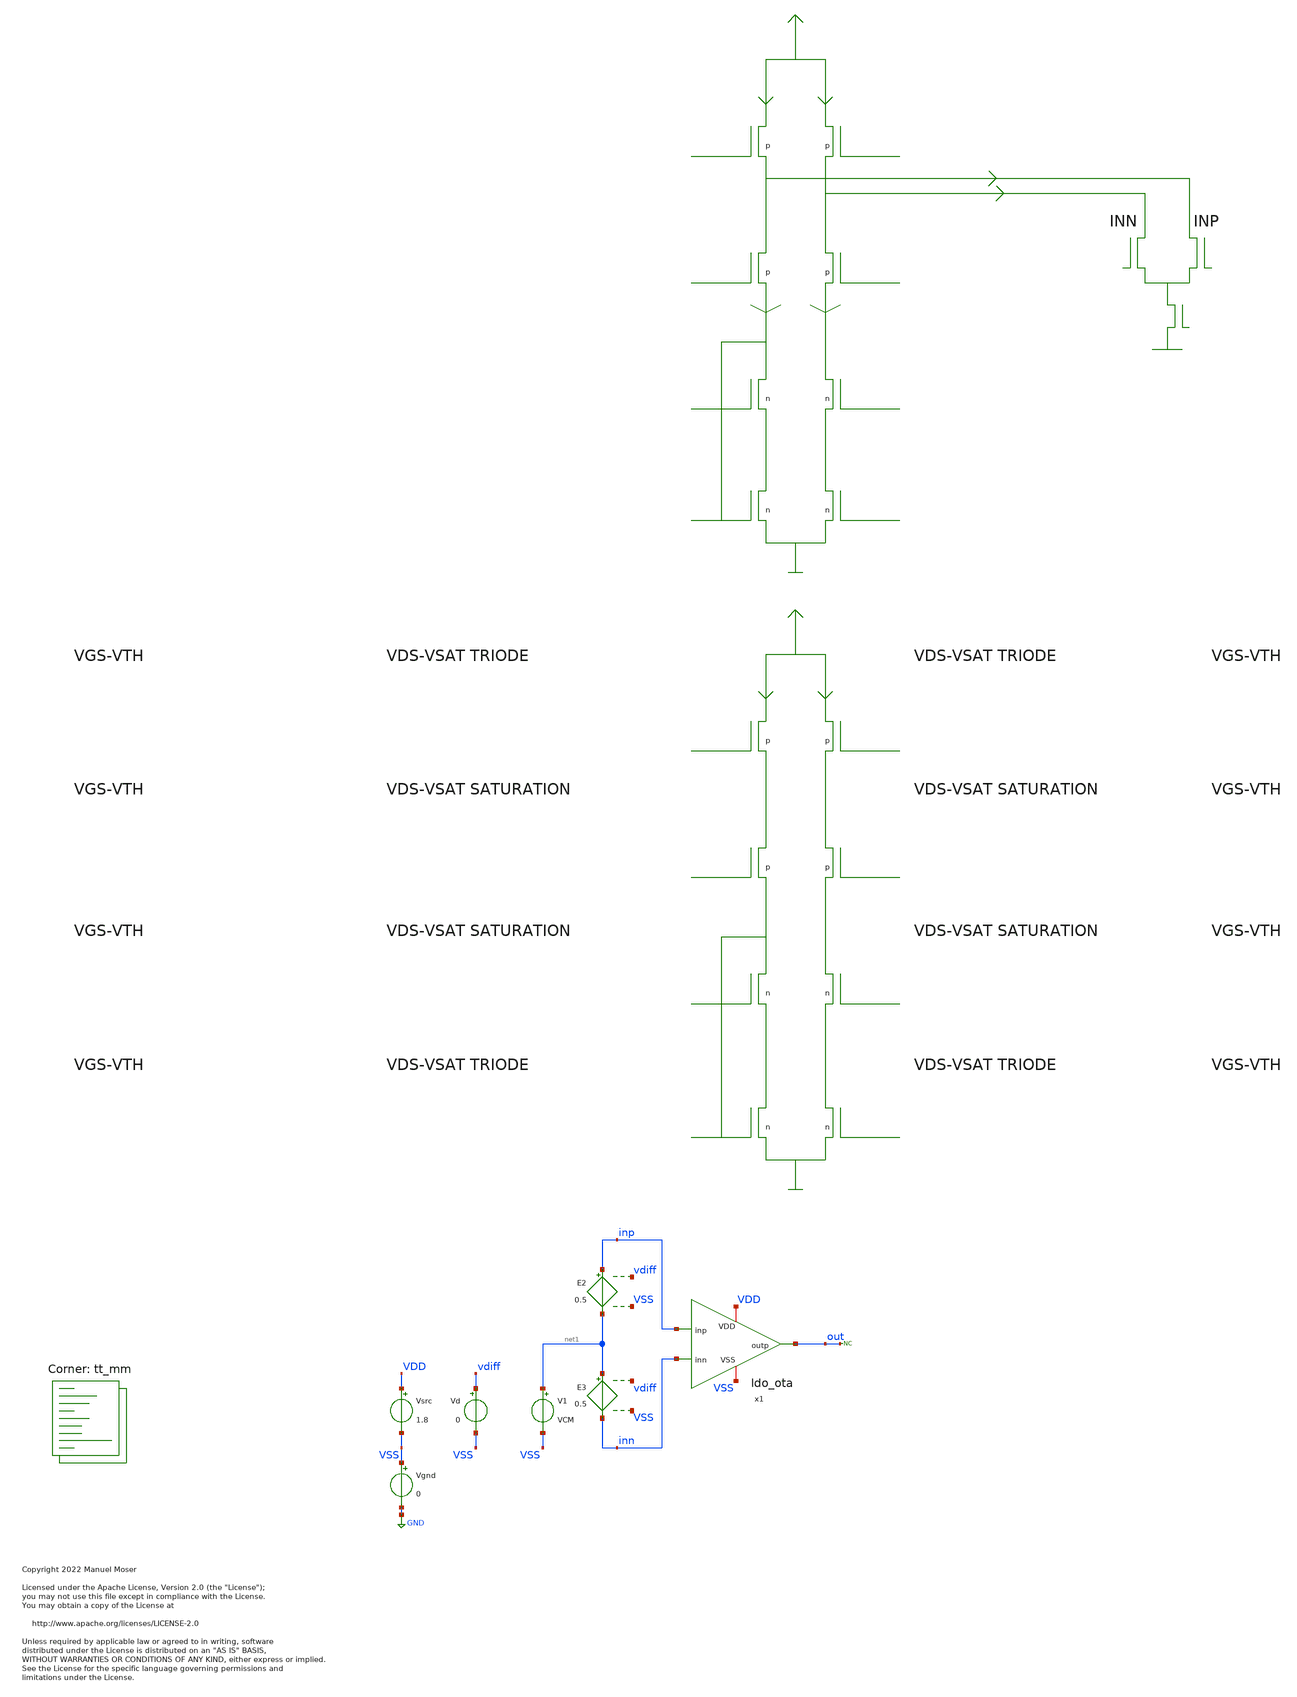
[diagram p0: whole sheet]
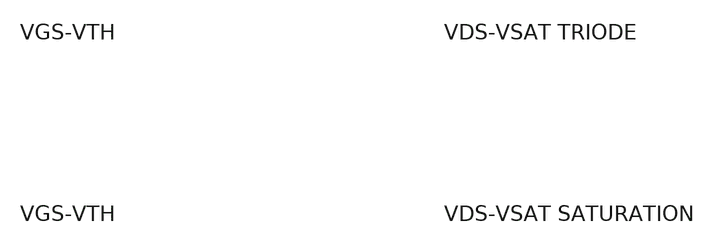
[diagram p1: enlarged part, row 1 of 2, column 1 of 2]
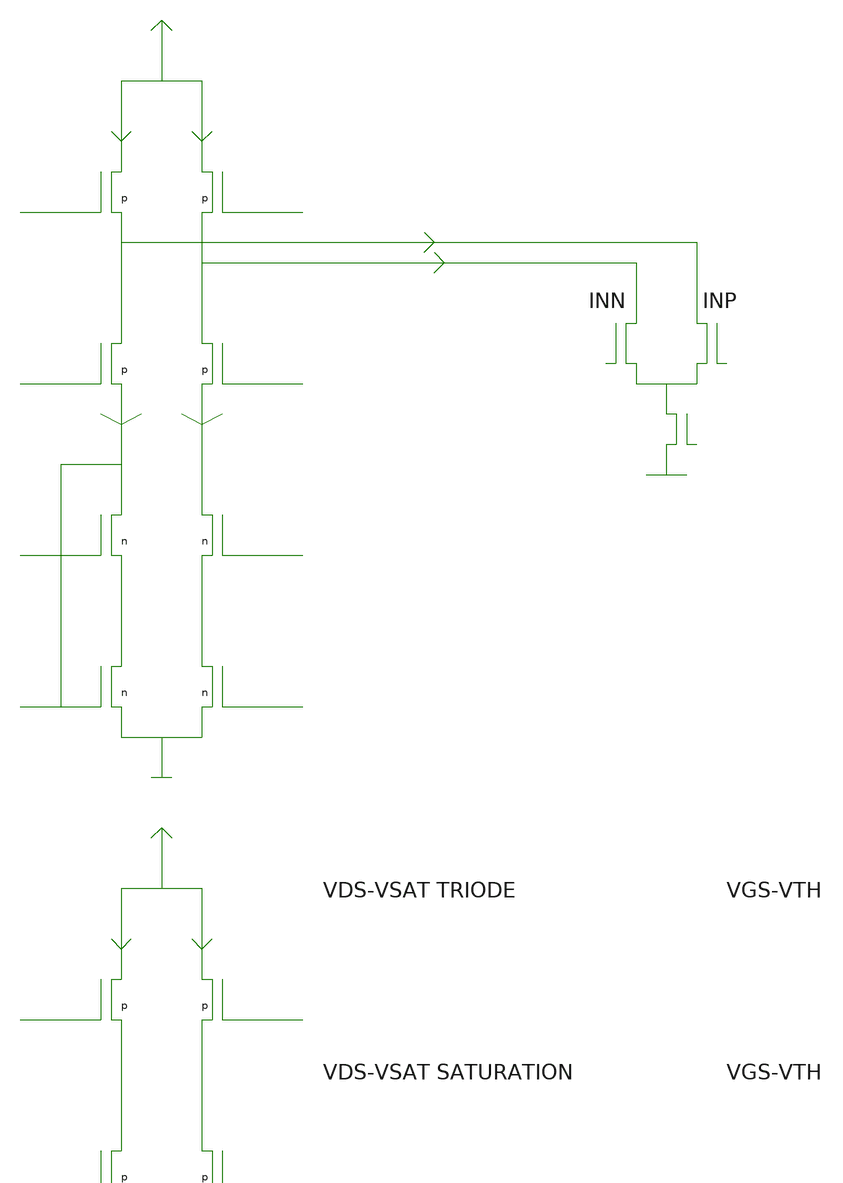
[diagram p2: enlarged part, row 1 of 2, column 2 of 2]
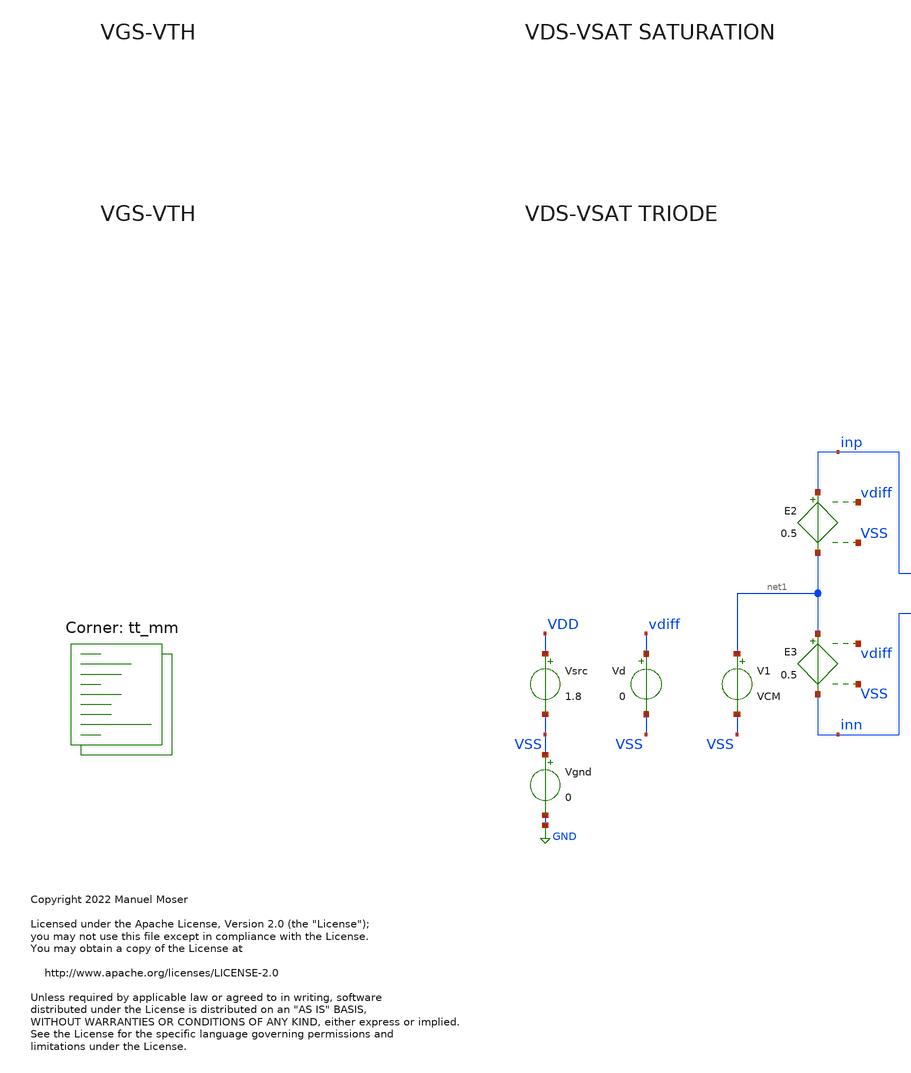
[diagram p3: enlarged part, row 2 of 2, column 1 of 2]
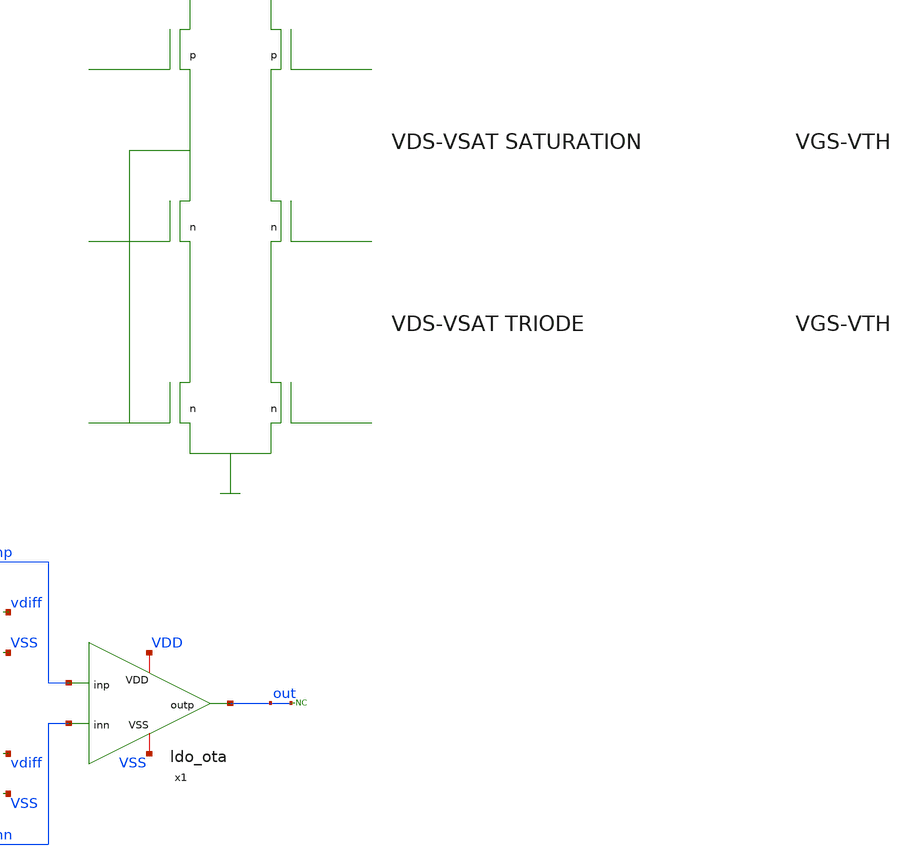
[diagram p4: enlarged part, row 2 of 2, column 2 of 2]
** sch_path: xschem/ldo_ota_tb.sch
* Copyright 2022 Manuel Moser
* Licensed under the Apache License, Version 2.0 (the "License");
**.subckt ldo_ota_tb
x1 VDD inp out inn VSS ldo_ota
V1 net1 VSS VCM
Vd vdiff VSS 0
Vsrc VDD VSS 1.8
* noconn out
E2 inp net1 vdiff VSS 0.5
E3 net1 inn vdiff VSS 0.5
Vgnd VSS GND 0
**** begin user architecture code



.temp 27
.options savecurrents

.param vcm = 0.9

.save all
 + @m.x1.x1.xmn1.msky130_fd_pr__nfet_01v8_lvt[vgs] @m.x1.x1.xmn1.msky130_fd_pr__nfet_01v8_lvt[vth]
+ @m.x1.x1.xmn1.msky130_fd_pr__nfet_01v8_lvt[vds] @m.x1.x1.xmn1.msky130_fd_pr__nfet_01v8_lvt[vdsat] @m.x1.x1.xmn1.msky130_fd_pr__nfet_01v8_lvt[id]
 + @m.x1.x1.xmn2.msky130_fd_pr__nfet_01v8_lvt[vgs] @m.x1.x1.xmn2.msky130_fd_pr__nfet_01v8_lvt[vth]
+ @m.x1.x1.xmn2.msky130_fd_pr__nfet_01v8_lvt[vds] @m.x1.x1.xmn2.msky130_fd_pr__nfet_01v8_lvt[vdsat] @m.x1.x1.xmn2.msky130_fd_pr__nfet_01v8_lvt[id]
 + @m.x1.x1.xmn3.msky130_fd_pr__nfet_01v8_lvt[vgs] @m.x1.x1.xmn3.msky130_fd_pr__nfet_01v8_lvt[vth]
+ @m.x1.x1.xmn3.msky130_fd_pr__nfet_01v8_lvt[vds] @m.x1.x1.xmn3.msky130_fd_pr__nfet_01v8_lvt[vdsat] @m.x1.x1.xmn3.msky130_fd_pr__nfet_01v8_lvt[id]
 + @m.x1.x1.xmn4.msky130_fd_pr__nfet_01v8_lvt[vgs] @m.x1.x1.xmn4.msky130_fd_pr__nfet_01v8_lvt[vth]
+ @m.x1.x1.xmn4.msky130_fd_pr__nfet_01v8_lvt[vds] @m.x1.x1.xmn4.msky130_fd_pr__nfet_01v8_lvt[vdsat] @m.x1.x1.xmn4.msky130_fd_pr__nfet_01v8_lvt[id]
 + @m.x1.x1.xmn5.msky130_fd_pr__nfet_01v8_lvt[vgs] @m.x1.x1.xmn5.msky130_fd_pr__nfet_01v8_lvt[vth]
+ @m.x1.x1.xmn5.msky130_fd_pr__nfet_01v8_lvt[vds] @m.x1.x1.xmn5.msky130_fd_pr__nfet_01v8_lvt[vdsat] @m.x1.x1.xmn5.msky130_fd_pr__nfet_01v8_lvt[id]
 + @m.x1.x1.xmn6.msky130_fd_pr__nfet_01v8_lvt[vgs] @m.x1.x1.xmn6.msky130_fd_pr__nfet_01v8_lvt[vth]
+ @m.x1.x1.xmn6.msky130_fd_pr__nfet_01v8_lvt[vds] @m.x1.x1.xmn6.msky130_fd_pr__nfet_01v8_lvt[vdsat] @m.x1.x1.xmn6.msky130_fd_pr__nfet_01v8_lvt[id]
 + @m.x1.x1.xmn7.msky130_fd_pr__nfet_01v8_lvt[vgs] @m.x1.x1.xmn7.msky130_fd_pr__nfet_01v8_lvt[vth]
+ @m.x1.x1.xmn7.msky130_fd_pr__nfet_01v8_lvt[vds] @m.x1.x1.xmn7.msky130_fd_pr__nfet_01v8_lvt[vdsat] @m.x1.x1.xmn7.msky130_fd_pr__nfet_01v8_lvt[id]
 + @m.x1.x1.xmp1.msky130_fd_pr__pfet_01v8_lvt[vgs] @m.x1.x1.xmp1.msky130_fd_pr__pfet_01v8_lvt[vth]
+ @m.x1.x1.xmp1.msky130_fd_pr__pfet_01v8_lvt[vds] @m.x1.x1.xmp1.msky130_fd_pr__pfet_01v8_lvt[vdsat] @m.x1.x1.xmp1.msky130_fd_pr__pfet_01v8_lvt[id]
 + @m.x1.x1.xmp2.msky130_fd_pr__pfet_01v8_lvt[vgs] @m.x1.x1.xmp2.msky130_fd_pr__pfet_01v8_lvt[vth]
+ @m.x1.x1.xmp2.msky130_fd_pr__pfet_01v8_lvt[vds] @m.x1.x1.xmp2.msky130_fd_pr__pfet_01v8_lvt[vdsat] @m.x1.x1.xmp2.msky130_fd_pr__pfet_01v8_lvt[id]
 + @m.x1.x1.xmp3.msky130_fd_pr__pfet_01v8_lvt[vgs] @m.x1.x1.xmp3.msky130_fd_pr__pfet_01v8_lvt[vth]
+ @m.x1.x1.xmp3.msky130_fd_pr__pfet_01v8_lvt[vds] @m.x1.x1.xmp3.msky130_fd_pr__pfet_01v8_lvt[vdsat] @m.x1.x1.xmp3.msky130_fd_pr__pfet_01v8_lvt[id]
 + @m.x1.x1.xmp4.msky130_fd_pr__pfet_01v8_lvt[vgs] @m.x1.x1.xmp4.msky130_fd_pr__pfet_01v8_lvt[vth]
+ @m.x1.x1.xmp4.msky130_fd_pr__pfet_01v8_lvt[vds] @m.x1.x1.xmp4.msky130_fd_pr__pfet_01v8_lvt[vdsat] @m.x1.x1.xmp4.msky130_fd_pr__pfet_01v8_lvt[id]

.control
set num_threads = 12
write results.raw
set appendwrite

repeat 20
  reset
  dc vd -50m 50m 0.1m temp -30 60 90
  *dc temp -30 60 1

write results.raw out x1.bias1 x1.bias2 x1.bias3 x1.bias4
 + @m.x1.x1.xmn1.msky130_fd_pr__nfet_01v8_lvt[vgs] @m.x1.x1.xmn1.msky130_fd_pr__nfet_01v8_lvt[vth]
+ @m.x1.x1.xmn1.msky130_fd_pr__nfet_01v8_lvt[vds] @m.x1.x1.xmn1.msky130_fd_pr__nfet_01v8_lvt[vdsat] @m.x1.x1.xmn1.msky130_fd_pr__nfet_01v8_lvt[id]
 + @m.x1.x1.xmn2.msky130_fd_pr__nfet_01v8_lvt[vgs] @m.x1.x1.xmn2.msky130_fd_pr__nfet_01v8_lvt[vth]
+ @m.x1.x1.xmn2.msky130_fd_pr__nfet_01v8_lvt[vds] @m.x1.x1.xmn2.msky130_fd_pr__nfet_01v8_lvt[vdsat] @m.x1.x1.xmn2.msky130_fd_pr__nfet_01v8_lvt[id]
 + @m.x1.x1.xmn3.msky130_fd_pr__nfet_01v8_lvt[vgs] @m.x1.x1.xmn3.msky130_fd_pr__nfet_01v8_lvt[vth]
+ @m.x1.x1.xmn3.msky130_fd_pr__nfet_01v8_lvt[vds] @m.x1.x1.xmn3.msky130_fd_pr__nfet_01v8_lvt[vdsat] @m.x1.x1.xmn3.msky130_fd_pr__nfet_01v8_lvt[id]
 + @m.x1.x1.xmn4.msky130_fd_pr__nfet_01v8_lvt[vgs] @m.x1.x1.xmn4.msky130_fd_pr__nfet_01v8_lvt[vth]
+ @m.x1.x1.xmn4.msky130_fd_pr__nfet_01v8_lvt[vds] @m.x1.x1.xmn4.msky130_fd_pr__nfet_01v8_lvt[vdsat] @m.x1.x1.xmn4.msky130_fd_pr__nfet_01v8_lvt[id]
 + @m.x1.x1.xmn5.msky130_fd_pr__nfet_01v8_lvt[vgs] @m.x1.x1.xmn5.msky130_fd_pr__nfet_01v8_lvt[vth]
+ @m.x1.x1.xmn5.msky130_fd_pr__nfet_01v8_lvt[vds] @m.x1.x1.xmn5.msky130_fd_pr__nfet_01v8_lvt[vdsat] @m.x1.x1.xmn5.msky130_fd_pr__nfet_01v8_lvt[id]
 + @m.x1.x1.xmn6.msky130_fd_pr__nfet_01v8_lvt[vgs] @m.x1.x1.xmn6.msky130_fd_pr__nfet_01v8_lvt[vth]
+ @m.x1.x1.xmn6.msky130_fd_pr__nfet_01v8_lvt[vds] @m.x1.x1.xmn6.msky130_fd_pr__nfet_01v8_lvt[vdsat] @m.x1.x1.xmn6.msky130_fd_pr__nfet_01v8_lvt[id]
 + @m.x1.x1.xmn7.msky130_fd_pr__nfet_01v8_lvt[vgs] @m.x1.x1.xmn7.msky130_fd_pr__nfet_01v8_lvt[vth]
+ @m.x1.x1.xmn7.msky130_fd_pr__nfet_01v8_lvt[vds] @m.x1.x1.xmn7.msky130_fd_pr__nfet_01v8_lvt[vdsat] @m.x1.x1.xmn7.msky130_fd_pr__nfet_01v8_lvt[id]
 + @m.x1.x1.xmp1.msky130_fd_pr__pfet_01v8_lvt[vgs] @m.x1.x1.xmp1.msky130_fd_pr__pfet_01v8_lvt[vth]
+ @m.x1.x1.xmp1.msky130_fd_pr__pfet_01v8_lvt[vds] @m.x1.x1.xmp1.msky130_fd_pr__pfet_01v8_lvt[vdsat] @m.x1.x1.xmp1.msky130_fd_pr__pfet_01v8_lvt[id]
 + @m.x1.x1.xmp2.msky130_fd_pr__pfet_01v8_lvt[vgs] @m.x1.x1.xmp2.msky130_fd_pr__pfet_01v8_lvt[vth]
+ @m.x1.x1.xmp2.msky130_fd_pr__pfet_01v8_lvt[vds] @m.x1.x1.xmp2.msky130_fd_pr__pfet_01v8_lvt[vdsat] @m.x1.x1.xmp2.msky130_fd_pr__pfet_01v8_lvt[id]
 + @m.x1.x1.xmp3.msky130_fd_pr__pfet_01v8_lvt[vgs] @m.x1.x1.xmp3.msky130_fd_pr__pfet_01v8_lvt[vth]
+ @m.x1.x1.xmp3.msky130_fd_pr__pfet_01v8_lvt[vds] @m.x1.x1.xmp3.msky130_fd_pr__pfet_01v8_lvt[vdsat] @m.x1.x1.xmp3.msky130_fd_pr__pfet_01v8_lvt[id]
 + @m.x1.x1.xmp4.msky130_fd_pr__pfet_01v8_lvt[vgs] @m.x1.x1.xmp4.msky130_fd_pr__pfet_01v8_lvt[vth]
+ @m.x1.x1.xmp4.msky130_fd_pr__pfet_01v8_lvt[vds] @m.x1.x1.xmp4.msky130_fd_pr__pfet_01v8_lvt[vdsat] @m.x1.x1.xmp4.msky130_fd_pr__pfet_01v8_lvt[id]


end

.endc




.lib $::SKYWATER_MODELS/sky130.lib.spice tt_mm
**** end user architecture code
**.ends

* expanding   symbol:  ldo_ota.sym # of pins=5
** sym_path: xschem/ldo_ota.sym
** sch_path: xschem/ldo_ota.sch
.subckt ldo_ota VDD inp outp inn VSS
*.iopin VDD
*.iopin VSS
*.ipin inp
*.ipin inn
*.opin outp
x1 VDD inp inn bias1 bias2 bias3 outp VSS bias4 ldo_fc
x2 net1 bias2 VDD VSS bias1 net6 ldo_isource
XM10 net2 bias2 VDD VDD sky130_fd_pr__pfet_01v8_lvt L=8 W='0.55 * 1 ' nf=1 ad='int((nf+1)/2) * W / nf * 0.29'
+ as='int((nf+2)/2) * W / nf * 0.29' pd='2*int((nf+1)/2) * (W / nf + 0.29)' ps='2*int((nf+2)/2) * (W / nf + 0.29)'
+ nrd='0.29 / W ' nrs='0.29 / W ' sa=0 sb=0 sd=0 mult=1 m=1
XM12 bias2 bias2 net2 VDD sky130_fd_pr__pfet_01v8_lvt L=8 W='0.55 * 9 ' nf=9 ad='int((nf+1)/2) * W / nf * 0.29'
+ as='int((nf+2)/2) * W / nf * 0.29' pd='2*int((nf+1)/2) * (W / nf + 0.29)' ps='2*int((nf+2)/2) * (W / nf + 0.29)'
+ nrd='0.29 / W ' nrs='0.29 / W ' sa=0 sb=0 sd=0 mult=1 m=1
* noconn #net1
XM1 net3 bias1 VDD VDD sky130_fd_pr__pfet_01v8_lvt L=8 W='0.55 * 3 ' nf=3 ad='int((nf+1)/2) * W / nf * 0.29'
+ as='int((nf+2)/2) * W / nf * 0.29' pd='2*int((nf+1)/2) * (W / nf + 0.29)' ps='2*int((nf+2)/2) * (W / nf + 0.29)'
+ nrd='0.29 / W ' nrs='0.29 / W ' sa=0 sb=0 sd=0 mult=1 m=1
XM2 bias1 bias2 net3 VDD sky130_fd_pr__pfet_01v8_lvt L=8 W='0.55 * 9 ' nf=9 ad='int((nf+1)/2) * W / nf * 0.29'
+ as='int((nf+2)/2) * W / nf * 0.29' pd='2*int((nf+1)/2) * (W / nf + 0.29)' ps='2*int((nf+2)/2) * (W / nf + 0.29)'
+ nrd='0.29 / W ' nrs='0.29 / W ' sa=0 sb=0 sd=0 mult=1 m=1
XM3 net4 bias1 VDD VDD sky130_fd_pr__pfet_01v8_lvt L=8 W='0.55 * 3 ' nf=3 ad='int((nf+1)/2) * W / nf * 0.29'
+ as='int((nf+2)/2) * W / nf * 0.29' pd='2*int((nf+1)/2) * (W / nf + 0.29)' ps='2*int((nf+2)/2) * (W / nf + 0.29)'
+ nrd='0.29 / W ' nrs='0.29 / W ' sa=0 sb=0 sd=0 mult=1 m=1
XM4 bias3 bias2 net4 VDD sky130_fd_pr__pfet_01v8_lvt L=8 W='0.55 * 9 ' nf=9 ad='int((nf+1)/2) * W / nf * 0.29'
+ as='int((nf+2)/2) * W / nf * 0.29' pd='2*int((nf+1)/2) * (W / nf + 0.29)' ps='2*int((nf+2)/2) * (W / nf + 0.29)'
+ nrd='0.29 / W ' nrs='0.29 / W ' sa=0 sb=0 sd=0 mult=1 m=1
XM5 net5 bias1 VDD VDD sky130_fd_pr__pfet_01v8_lvt L=8 W='0.55 * 3 ' nf=3 ad='int((nf+1)/2) * W / nf * 0.29'
+ as='int((nf+2)/2) * W / nf * 0.29' pd='2*int((nf+1)/2) * (W / nf + 0.29)' ps='2*int((nf+2)/2) * (W / nf + 0.29)'
+ nrd='0.29 / W ' nrs='0.29 / W ' sa=0 sb=0 sd=0 mult=1 m=1
XM8 bias4 bias2 net5 VDD sky130_fd_pr__pfet_01v8_lvt L=8 W='0.55 * 9 ' nf=9 ad='int((nf+1)/2) * W / nf * 0.29'
+ as='int((nf+2)/2) * W / nf * 0.29' pd='2*int((nf+1)/2) * (W / nf + 0.29)' ps='2*int((nf+2)/2) * (W / nf + 0.29)'
+ nrd='0.29 / W ' nrs='0.29 / W ' sa=0 sb=0 sd=0 mult=1 m=1
* noconn #net6
XM9 bias3 bias3 net7 VSS sky130_fd_pr__nfet_01v8_lvt L=4 W='0.55 * 9 ' nf=9 ad='int((nf+1)/2) * W / nf * 0.29'
+ as='int((nf+2)/2) * W / nf * 0.29' pd='2*int((nf+1)/2) * (W / nf + 0.29)' ps='2*int((nf+2)/2) * (W / nf + 0.29)'
+ nrd='0.29 / W ' nrs='0.29 / W ' sa=0 sb=0 sd=0 mult=1 m=1
XM11 net7 bias3 VSS VSS sky130_fd_pr__nfet_01v8_lvt L=4 W='0.55 * 1 ' nf=1 ad='int((nf+1)/2) * W / nf * 0.29'
+ as='int((nf+2)/2) * W / nf * 0.29' pd='2*int((nf+1)/2) * (W / nf + 0.29)' ps='2*int((nf+2)/2) * (W / nf + 0.29)'
+ nrd='0.29 / W ' nrs='0.29 / W ' sa=0 sb=0 sd=0 mult=1 m=1
XM13 bias4 bias3 net8 VSS sky130_fd_pr__nfet_01v8_lvt L=4 W='0.55 * 9 ' nf=9 ad='int((nf+1)/2) * W / nf * 0.29'
+ as='int((nf+2)/2) * W / nf * 0.29' pd='2*int((nf+1)/2) * (W / nf + 0.29)' ps='2*int((nf+2)/2) * (W / nf + 0.29)'
+ nrd='0.29 / W ' nrs='0.29 / W ' sa=0 sb=0 sd=0 mult=1 m=1
XM14 net8 bias4 VSS VSS sky130_fd_pr__nfet_01v8_lvt L=4 W='0.55 * 3 ' nf=3 ad='int((nf+1)/2) * W / nf * 0.29'
+ as='int((nf+2)/2) * W / nf * 0.29' pd='2*int((nf+1)/2) * (W / nf + 0.29)' ps='2*int((nf+2)/2) * (W / nf + 0.29)'
+ nrd='0.29 / W ' nrs='0.29 / W ' sa=0 sb=0 sd=0 mult=1 m=1
.ends


* expanding   symbol:  ldo_fc.sym # of pins=9
** sym_path: xschem/ldo_fc.sym
** sch_path: xschem/ldo_fc.sch
.subckt ldo_fc VDD inp inn bias1 bias2 bias3 outp VSS bias4
*.iopin VSS
*.iopin VDD
*.ipin inp
*.ipin inn
*.ipin bias1
*.opin outp
*.ipin bias2
*.ipin bias3
*.ipin bias4
XMN4 outp bias3 net1 VSS sky130_fd_pr__nfet_01v8_lvt L=4 W='0.55 * 9 ' nf=9 ad='int((nf+1)/2) * W / nf * 0.29'
+ as='int((nf+2)/2) * W / nf * 0.29' pd='2*int((nf+1)/2) * (W / nf + 0.29)' ps='2*int((nf+2)/2) * (W / nf + 0.29)'
+ nrd='0.29 / W ' nrs='0.29 / W ' sa=0 sb=0 sd=0 mult=8 m=8
XMN7 net1 net3 VSS VSS sky130_fd_pr__nfet_01v8_lvt L=4 W='0.55 * 3 ' nf=3 ad='int((nf+1)/2) * W / nf * 0.29'
+ as='int((nf+2)/2) * W / nf * 0.29' pd='2*int((nf+1)/2) * (W / nf + 0.29)' ps='2*int((nf+2)/2) * (W / nf + 0.29)'
+ nrd='0.29 / W ' nrs='0.29 / W ' sa=0 sb=0 sd=0 mult=8 m=8
XMN3 net3 bias3 net2 VSS sky130_fd_pr__nfet_01v8_lvt L=4 W='0.55 * 9 ' nf=9 ad='int((nf+1)/2) * W / nf * 0.29'
+ as='int((nf+2)/2) * W / nf * 0.29' pd='2*int((nf+1)/2) * (W / nf + 0.29)' ps='2*int((nf+2)/2) * (W / nf + 0.29)'
+ nrd='0.29 / W ' nrs='0.29 / W ' sa=0 sb=0 sd=0 mult=8 m=8
XMN6 net2 net3 VSS VSS sky130_fd_pr__nfet_01v8_lvt L=4 W='0.55 * 3 ' nf=3 ad='int((nf+1)/2) * W / nf * 0.29'
+ as='int((nf+2)/2) * W / nf * 0.29' pd='2*int((nf+1)/2) * (W / nf + 0.29)' ps='2*int((nf+2)/2) * (W / nf + 0.29)'
+ nrd='0.29 / W ' nrs='0.29 / W ' sa=0 sb=0 sd=0 mult=8 m=8
XMP4 outp bias2 net5 VDD sky130_fd_pr__pfet_01v8_lvt L=8 W='0.55 * 9 ' nf=9 ad='int((nf+1)/2) * W / nf * 0.29'
+ as='int((nf+2)/2) * W / nf * 0.29' pd='2*int((nf+1)/2) * (W / nf + 0.29)' ps='2*int((nf+2)/2) * (W / nf + 0.29)'
+ nrd='0.29 / W ' nrs='0.29 / W ' sa=0 sb=0 sd=0 mult=8 m=8
XMP2 net5 bias1 VDD VDD sky130_fd_pr__pfet_01v8_lvt L=8 W='0.55 * 3 ' nf=3 ad='int((nf+1)/2) * W / nf * 0.29'
+ as='int((nf+2)/2) * W / nf * 0.29' pd='2*int((nf+1)/2) * (W / nf + 0.29)' ps='2*int((nf+2)/2) * (W / nf + 0.29)'
+ nrd='0.29 / W ' nrs='0.29 / W ' sa=0 sb=0 sd=0 mult=15 m=15
XMP3 net3 bias2 net4 VDD sky130_fd_pr__pfet_01v8_lvt L=8 W='0.55 * 9 ' nf=9 ad='int((nf+1)/2) * W / nf * 0.29'
+ as='int((nf+2)/2) * W / nf * 0.29' pd='2*int((nf+1)/2) * (W / nf + 0.29)' ps='2*int((nf+2)/2) * (W / nf + 0.29)'
+ nrd='0.29 / W ' nrs='0.29 / W ' sa=0 sb=0 sd=0 mult=8 m=8
XMP1 net4 bias1 VDD VDD sky130_fd_pr__pfet_01v8_lvt L=8 W='0.55 * 3 ' nf=3 ad='int((nf+1)/2) * W / nf * 0.29'
+ as='int((nf+2)/2) * W / nf * 0.29' pd='2*int((nf+1)/2) * (W / nf + 0.29)' ps='2*int((nf+2)/2) * (W / nf + 0.29)'
+ nrd='0.29 / W ' nrs='0.29 / W ' sa=0 sb=0 sd=0 mult=15 m=15
XMN5 net6 bias4 VSS VSS sky130_fd_pr__nfet_01v8_lvt L=4 W='0.55 * 3 ' nf=3 ad='int((nf+1)/2) * W / nf * 0.29'
+ as='int((nf+2)/2) * W / nf * 0.29' pd='2*int((nf+1)/2) * (W / nf + 0.29)' ps='2*int((nf+2)/2) * (W / nf + 0.29)'
+ nrd='0.29 / W ' nrs='0.29 / W ' sa=0 sb=0 sd=0 mult=14 m=14
XMN1 net4 inp net6 VSS sky130_fd_pr__nfet_01v8_lvt L=0.25 W='7 * 20 ' nf=20 ad='int((nf+1)/2) * W / nf * 0.29'
+ as='int((nf+2)/2) * W / nf * 0.29' pd='2*int((nf+1)/2) * (W / nf + 0.29)' ps='2*int((nf+2)/2) * (W / nf + 0.29)'
+ nrd='0.29 / W ' nrs='0.29 / W ' sa=0 sb=0 sd=0 mult=1 m=1
XMN2 net5 inn net6 VSS sky130_fd_pr__nfet_01v8_lvt L=0.25 W='7 * 20 ' nf=20 ad='int((nf+1)/2) * W / nf * 0.29'
+ as='int((nf+2)/2) * W / nf * 0.29' pd='2*int((nf+1)/2) * (W / nf + 0.29)' ps='2*int((nf+2)/2) * (W / nf + 0.29)'
+ nrd='0.29 / W ' nrs='0.29 / W ' sa=0 sb=0 sd=0 mult=1 m=1
.ends


* expanding   symbol:  ldo_isource.sym # of pins=6
** sym_path: xschem/ldo_isource.sym
** sch_path: xschem/ldo_isource.sch
.subckt ldo_isource curr_p2 curr_n1 VDD VSS curr_n2 curr_p1
*.iopin VDD
*.iopin VSS
*.ipin curr_n1
*.opin curr_p1
*.ipin curr_n2
*.opin curr_p2
XMP2 VGP VGP net4 VDD sky130_fd_pr__pfet_01v8_lvt L=8 W='0.55 * 7 ' nf=7 ad='int((nf+1)/2) * W / nf * 0.29'
+ as='int((nf+2)/2) * W / nf * 0.29' pd='2*int((nf+1)/2) * (W / nf + 0.29)' ps='2*int((nf+2)/2) * (W / nf + 0.29)'
+ nrd='0.29 / W ' nrs='0.29 / W ' sa=0 sb=0 sd=0 mult=1 m=1
XMP1 VGN VGP net3 VDD sky130_fd_pr__pfet_01v8_lvt L=8 W='0.55 * 7 ' nf=7 ad='int((nf+1)/2) * W / nf * 0.29'
+ as='int((nf+2)/2) * W / nf * 0.29' pd='2*int((nf+1)/2) * (W / nf + 0.29)' ps='2*int((nf+2)/2) * (W / nf + 0.29)'
+ nrd='0.29 / W ' nrs='0.29 / W ' sa=0 sb=0 sd=0 mult=1 m=1
XMN1 VGN VGN net1 VSS sky130_fd_pr__nfet_01v8_lvt L=8 W='7 * 1 ' nf=1 ad='int((nf+1)/2) * W / nf * 0.29'
+ as='int((nf+2)/2) * W / nf * 0.29' pd='2*int((nf+1)/2) * (W / nf + 0.29)' ps='2*int((nf+2)/2) * (W / nf + 0.29)'
+ nrd='0.29 / W ' nrs='0.29 / W ' sa=0 sb=0 sd=0 mult=1 m=1
XMN2 VGP VGN net2 VSS sky130_fd_pr__nfet_01v8_lvt L=8 W='7 * 1 ' nf=1 ad='int((nf+1)/2) * W / nf * 0.29'
+ as='int((nf+2)/2) * W / nf * 0.29' pd='2*int((nf+1)/2) * (W / nf + 0.29)' ps='2*int((nf+2)/2) * (W / nf + 0.29)'
+ nrd='0.29 / W ' nrs='0.29 / W ' sa=0 sb=0 sd=0 mult=5 m=5
XMN3 net1 VGN VSS VSS sky130_fd_pr__nfet_01v8_lvt L=8 W='7 * 1 ' nf=1 ad='int((nf+1)/2) * W / nf * 0.29'
+ as='int((nf+2)/2) * W / nf * 0.29' pd='2*int((nf+1)/2) * (W / nf + 0.29)' ps='2*int((nf+2)/2) * (W / nf + 0.29)'
+ nrd='0.29 / W ' nrs='0.29 / W ' sa=0 sb=0 sd=0 mult=1 m=1
XMN4 net2 VGN Vref VSS sky130_fd_pr__nfet_01v8_lvt L=8 W='7 * 1 ' nf=1 ad='int((nf+1)/2) * W / nf * 0.29'
+ as='int((nf+2)/2) * W / nf * 0.29' pd='2*int((nf+1)/2) * (W / nf + 0.29)' ps='2*int((nf+2)/2) * (W / nf + 0.29)'
+ nrd='0.29 / W ' nrs='0.29 / W ' sa=0 sb=0 sd=0 mult=5 m=5
XMP4 net3 VGP VDD VDD sky130_fd_pr__pfet_01v8_lvt L=8 W='0.55 * 7 ' nf=7 ad='int((nf+1)/2) * W / nf * 0.29'
+ as='int((nf+2)/2) * W / nf * 0.29' pd='2*int((nf+1)/2) * (W / nf + 0.29)' ps='2*int((nf+2)/2) * (W / nf + 0.29)'
+ nrd='0.29 / W ' nrs='0.29 / W ' sa=0 sb=0 sd=0 mult=1 m=1
XMP5 net4 VGP VDD VDD sky130_fd_pr__pfet_01v8_lvt L=8 W='0.55 * 7 ' nf=7 ad='int((nf+1)/2) * W / nf * 0.29'
+ as='int((nf+2)/2) * W / nf * 0.29' pd='2*int((nf+1)/2) * (W / nf + 0.29)' ps='2*int((nf+2)/2) * (W / nf + 0.29)'
+ nrd='0.29 / W ' nrs='0.29 / W ' sa=0 sb=0 sd=0 mult=1 m=1
XMP3 Vrefgate VGP net19 VDD sky130_fd_pr__pfet_01v8_lvt L=8 W='0.55 * 7 ' nf=7 ad='int((nf+1)/2) * W / nf * 0.29'
+ as='int((nf+2)/2) * W / nf * 0.29' pd='2*int((nf+1)/2) * (W / nf + 0.29)' ps='2*int((nf+2)/2) * (W / nf + 0.29)'
+ nrd='0.29 / W ' nrs='0.29 / W ' sa=0 sb=0 sd=0 mult=1 m=1
XM2 net5 Vrefgate net6 VSS sky130_fd_pr__nfet_01v8 L=4 W='1 * 1 ' nf=1 ad='int((nf+1)/2) * W / nf * 0.29'
+ as='int((nf+2)/2) * W / nf * 0.29' pd='2*int((nf+1)/2) * (W / nf + 0.29)' ps='2*int((nf+2)/2) * (W / nf + 0.29)'
+ nrd='0.29 / W ' nrs='0.29 / W ' sa=0 sb=0 sd=0 mult=1 m=1
XM3 net8 Vrefgate VSS VSS sky130_fd_pr__nfet_01v8 L=4 W='1 * 1 ' nf=1 ad='int((nf+1)/2) * W / nf * 0.29'
+ as='int((nf+2)/2) * W / nf * 0.29' pd='2*int((nf+1)/2) * (W / nf + 0.29)' ps='2*int((nf+2)/2) * (W / nf + 0.29)'
+ nrd='0.29 / W ' nrs='0.29 / W ' sa=0 sb=0 sd=0 mult=1 m=1
XM1 net7 Vrefgate net8 VSS sky130_fd_pr__nfet_01v8 L=4 W='1 * 1 ' nf=1 ad='int((nf+1)/2) * W / nf * 0.29'
+ as='int((nf+2)/2) * W / nf * 0.29' pd='2*int((nf+1)/2) * (W / nf + 0.29)' ps='2*int((nf+2)/2) * (W / nf + 0.29)'
+ nrd='0.29 / W ' nrs='0.29 / W ' sa=0 sb=0 sd=0 mult=1 m=1
XM4 net6 Vrefgate net7 VSS sky130_fd_pr__nfet_01v8 L=4 W='1 * 1 ' nf=1 ad='int((nf+1)/2) * W / nf * 0.29'
+ as='int((nf+2)/2) * W / nf * 0.29' pd='2*int((nf+1)/2) * (W / nf + 0.29)' ps='2*int((nf+2)/2) * (W / nf + 0.29)'
+ nrd='0.29 / W ' nrs='0.29 / W ' sa=0 sb=0 sd=0 mult=1 m=1
XMN5 net10 Vrefgate VSS VSS sky130_fd_pr__nfet_01v8_lvt L=4 W='1 * 1 ' nf=1 ad='int((nf+1)/2) * W / nf * 0.29'
+ as='int((nf+2)/2) * W / nf * 0.29' pd='2*int((nf+1)/2) * (W / nf + 0.29)' ps='2*int((nf+2)/2) * (W / nf + 0.29)'
+ nrd='0.29 / W ' nrs='0.29 / W ' sa=0 sb=0 sd=0 mult=1 m=1
XMN6 net14 Vrefgate net9 VSS sky130_fd_pr__nfet_01v8_lvt L=4 W='1 * 1 ' nf=1 ad='int((nf+1)/2) * W / nf * 0.29'
+ as='int((nf+2)/2) * W / nf * 0.29' pd='2*int((nf+1)/2) * (W / nf + 0.29)' ps='2*int((nf+2)/2) * (W / nf + 0.29)'
+ nrd='0.29 / W ' nrs='0.29 / W ' sa=0 sb=0 sd=0 mult=1 m=1
XMN9 net16 Vrefgate net14 VSS sky130_fd_pr__nfet_01v8_lvt L=4 W='1 * 1 ' nf=1 ad='int((nf+1)/2) * W / nf * 0.29'
+ as='int((nf+2)/2) * W / nf * 0.29' pd='2*int((nf+1)/2) * (W / nf + 0.29)' ps='2*int((nf+2)/2) * (W / nf + 0.29)'
+ nrd='0.29 / W ' nrs='0.29 / W ' sa=0 sb=0 sd=0 mult=1 m=1
XM5 Vrefgate Vrefgate net5 VSS sky130_fd_pr__nfet_01v8 L=4 W='1 * 1 ' nf=1 ad='int((nf+1)/2) * W / nf * 0.29'
+ as='int((nf+2)/2) * W / nf * 0.29' pd='2*int((nf+1)/2) * (W / nf + 0.29)' ps='2*int((nf+2)/2) * (W / nf + 0.29)'
+ nrd='0.29 / W ' nrs='0.29 / W ' sa=0 sb=0 sd=0 mult=1 m=1
XMN10 net11 Vrefgate net10 VSS sky130_fd_pr__nfet_01v8_lvt L=4 W='1 * 1 ' nf=1 ad='int((nf+1)/2) * W / nf * 0.29'
+ as='int((nf+2)/2) * W / nf * 0.29' pd='2*int((nf+1)/2) * (W / nf + 0.29)' ps='2*int((nf+2)/2) * (W / nf + 0.29)'
+ nrd='0.29 / W ' nrs='0.29 / W ' sa=0 sb=0 sd=0 mult=1 m=1
XMN11 net12 Vrefgate net11 VSS sky130_fd_pr__nfet_01v8_lvt L=4 W='1 * 1 ' nf=1 ad='int((nf+1)/2) * W / nf * 0.29'
+ as='int((nf+2)/2) * W / nf * 0.29' pd='2*int((nf+1)/2) * (W / nf + 0.29)' ps='2*int((nf+2)/2) * (W / nf + 0.29)'
+ nrd='0.29 / W ' nrs='0.29 / W ' sa=0 sb=0 sd=0 mult=1 m=1
XMN12 net13 Vrefgate net12 VSS sky130_fd_pr__nfet_01v8_lvt L=4 W='1 * 1 ' nf=1 ad='int((nf+1)/2) * W / nf * 0.29'
+ as='int((nf+2)/2) * W / nf * 0.29' pd='2*int((nf+1)/2) * (W / nf + 0.29)' ps='2*int((nf+2)/2) * (W / nf + 0.29)'
+ nrd='0.29 / W ' nrs='0.29 / W ' sa=0 sb=0 sd=0 mult=1 m=1
XMN13 net9 Vrefgate net13 VSS sky130_fd_pr__nfet_01v8_lvt L=4 W='1 * 1 ' nf=1 ad='int((nf+1)/2) * W / nf * 0.29'
+ as='int((nf+2)/2) * W / nf * 0.29' pd='2*int((nf+1)/2) * (W / nf + 0.29)' ps='2*int((nf+2)/2) * (W / nf + 0.29)'
+ nrd='0.29 / W ' nrs='0.29 / W ' sa=0 sb=0 sd=0 mult=1 m=1
XMN7 net18 Vrefgate net15 VSS sky130_fd_pr__nfet_01v8_lvt L=4 W='1 * 1 ' nf=1 ad='int((nf+1)/2) * W / nf * 0.29'
+ as='int((nf+2)/2) * W / nf * 0.29' pd='2*int((nf+1)/2) * (W / nf + 0.29)' ps='2*int((nf+2)/2) * (W / nf + 0.29)'
+ nrd='0.29 / W ' nrs='0.29 / W ' sa=0 sb=0 sd=0 mult=1 m=1
XMN8 Vref Vrefgate net18 VSS sky130_fd_pr__nfet_01v8_lvt L=4 W='1 * 1 ' nf=1 ad='int((nf+1)/2) * W / nf * 0.29'
+ as='int((nf+2)/2) * W / nf * 0.29' pd='2*int((nf+1)/2) * (W / nf + 0.29)' ps='2*int((nf+2)/2) * (W / nf + 0.29)'
+ nrd='0.29 / W ' nrs='0.29 / W ' sa=0 sb=0 sd=0 mult=1 m=1
XMN14 net17 Vrefgate net16 VSS sky130_fd_pr__nfet_01v8_lvt L=4 W='1 * 1 ' nf=1 ad='int((nf+1)/2) * W / nf * 0.29'
+ as='int((nf+2)/2) * W / nf * 0.29' pd='2*int((nf+1)/2) * (W / nf + 0.29)' ps='2*int((nf+2)/2) * (W / nf + 0.29)'
+ nrd='0.29 / W ' nrs='0.29 / W ' sa=0 sb=0 sd=0 mult=1 m=1
XMN15 net15 Vrefgate net17 VSS sky130_fd_pr__nfet_01v8_lvt L=4 W='1 * 1 ' nf=1 ad='int((nf+1)/2) * W / nf * 0.29'
+ as='int((nf+2)/2) * W / nf * 0.29' pd='2*int((nf+1)/2) * (W / nf + 0.29)' ps='2*int((nf+2)/2) * (W / nf + 0.29)'
+ nrd='0.29 / W ' nrs='0.29 / W ' sa=0 sb=0 sd=0 mult=1 m=1
XMP6 net19 VGP VDD VDD sky130_fd_pr__pfet_01v8_lvt L=8 W='0.55 * 7 ' nf=7 ad='int((nf+1)/2) * W / nf * 0.29'
+ as='int((nf+2)/2) * W / nf * 0.29' pd='2*int((nf+1)/2) * (W / nf + 0.29)' ps='2*int((nf+2)/2) * (W / nf + 0.29)'
+ nrd='0.29 / W ' nrs='0.29 / W ' sa=0 sb=0 sd=0 mult=1 m=1
XMP7 curr_p1 VGP net20 VDD sky130_fd_pr__pfet_01v8_lvt L=8 W='0.55 * 7 ' nf=7 ad='int((nf+1)/2) * W / nf * 0.29'
+ as='int((nf+2)/2) * W / nf * 0.29' pd='2*int((nf+1)/2) * (W / nf + 0.29)' ps='2*int((nf+2)/2) * (W / nf + 0.29)'
+ nrd='0.29 / W ' nrs='0.29 / W ' sa=0 sb=0 sd=0 mult=1 m=1
XMP8 net20 VGP VDD VDD sky130_fd_pr__pfet_01v8_lvt L=8 W='0.55 * 7 ' nf=7 ad='int((nf+1)/2) * W / nf * 0.29'
+ as='int((nf+2)/2) * W / nf * 0.29' pd='2*int((nf+1)/2) * (W / nf + 0.29)' ps='2*int((nf+2)/2) * (W / nf + 0.29)'
+ nrd='0.29 / W ' nrs='0.29 / W ' sa=0 sb=0 sd=0 mult=1 m=1
XMN16 curr_n1 VGN net21 VSS sky130_fd_pr__nfet_01v8_lvt L=8 W='7 * 1 ' nf=1 ad='int((nf+1)/2) * W / nf * 0.29'
+ as='int((nf+2)/2) * W / nf * 0.29' pd='2*int((nf+1)/2) * (W / nf + 0.29)' ps='2*int((nf+2)/2) * (W / nf + 0.29)'
+ nrd='0.29 / W ' nrs='0.29 / W ' sa=0 sb=0 sd=0 mult=1 m=1
XMN17 net21 VGN VSS VSS sky130_fd_pr__nfet_01v8_lvt L=8 W='7 * 1 ' nf=1 ad='int((nf+1)/2) * W / nf * 0.29'
+ as='int((nf+2)/2) * W / nf * 0.29' pd='2*int((nf+1)/2) * (W / nf + 0.29)' ps='2*int((nf+2)/2) * (W / nf + 0.29)'
+ nrd='0.29 / W ' nrs='0.29 / W ' sa=0 sb=0 sd=0 mult=1 m=1
XM6 VGP net22 VGN VSS sky130_fd_pr__nfet_01v8 L=4 W='1 * 1 ' nf=1 ad='int((nf+1)/2) * W / nf * 0.29'
+ as='int((nf+2)/2) * W / nf * 0.29' pd='2*int((nf+1)/2) * (W / nf + 0.29)' ps='2*int((nf+2)/2) * (W / nf + 0.29)'
+ nrd='0.29 / W ' nrs='0.29 / W ' sa=0 sb=0 sd=0 mult=1 m=1
XM7 net22 Vrefgate VSS VSS sky130_fd_pr__nfet_01v8 L=4 W='1 * 1 ' nf=1 ad='int((nf+1)/2) * W / nf * 0.29'
+ as='int((nf+2)/2) * W / nf * 0.29' pd='2*int((nf+1)/2) * (W / nf + 0.29)' ps='2*int((nf+2)/2) * (W / nf + 0.29)'
+ nrd='0.29 / W ' nrs='0.29 / W ' sa=0 sb=0 sd=0 mult=1 m=1
XC1 VDD net22 VSS sky130_fd_pr__cap_var_hvt W=2 L=2 VM=1 m=1
XMP9 curr_p2 VGP net23 VDD sky130_fd_pr__pfet_01v8_lvt L=8 W='0.55 * 7 ' nf=7 ad='int((nf+1)/2) * W / nf * 0.29'
+ as='int((nf+2)/2) * W / nf * 0.29' pd='2*int((nf+1)/2) * (W / nf + 0.29)' ps='2*int((nf+2)/2) * (W / nf + 0.29)'
+ nrd='0.29 / W ' nrs='0.29 / W ' sa=0 sb=0 sd=0 mult=1 m=1
XMP10 net23 VGP VDD VDD sky130_fd_pr__pfet_01v8_lvt L=8 W='0.55 * 7 ' nf=7 ad='int((nf+1)/2) * W / nf * 0.29'
+ as='int((nf+2)/2) * W / nf * 0.29' pd='2*int((nf+1)/2) * (W / nf + 0.29)' ps='2*int((nf+2)/2) * (W / nf + 0.29)'
+ nrd='0.29 / W ' nrs='0.29 / W ' sa=0 sb=0 sd=0 mult=1 m=1
XMN18 curr_n2 VGN net24 VSS sky130_fd_pr__nfet_01v8_lvt L=8 W='7 * 1 ' nf=1 ad='int((nf+1)/2) * W / nf * 0.29'
+ as='int((nf+2)/2) * W / nf * 0.29' pd='2*int((nf+1)/2) * (W / nf + 0.29)' ps='2*int((nf+2)/2) * (W / nf + 0.29)'
+ nrd='0.29 / W ' nrs='0.29 / W ' sa=0 sb=0 sd=0 mult=1 m=1
XMN19 net24 VGN VSS VSS sky130_fd_pr__nfet_01v8_lvt L=8 W='7 * 1 ' nf=1 ad='int((nf+1)/2) * W / nf * 0.29'
+ as='int((nf+2)/2) * W / nf * 0.29' pd='2*int((nf+1)/2) * (W / nf + 0.29)' ps='2*int((nf+2)/2) * (W / nf + 0.29)'
+ nrd='0.29 / W ' nrs='0.29 / W ' sa=0 sb=0 sd=0 mult=1 m=1
.ends

.GLOBAL GND
.end
